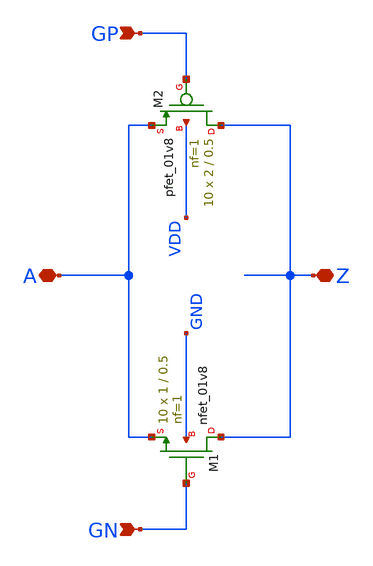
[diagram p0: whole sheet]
** sch_path: dacpassgate.sch
* Copyright 2021 Stefan Frederik Schippers
* Licensed under the Apache License, Version 2.0 (the "License");
* you may not use this file except in compliance with the License.
* You may obtain a copy of the License at
* https://www.apache.org/licenses/LICENSE-2.0
* Unless required by applicable law or agreed to in writing, software
* distributed under the License is distributed on an "AS IS" BASIS,
* WITHOUT WARRANTIES OR CONDITIONS OF ANY KIND, either express or implied.
* See the License for the specific language governing permissions and
* limitations under the License.
**.subckt dacpassgate A Z GP GN
*.iopin A
*.iopin Z
*.ipin GP
*.ipin GN
XM1 Z GN A GND sky130_fd_pr__nfet_01v8 L=0.5 W=1 nf=1 ad='int((nf+1)/2) * W/nf * 0.29' as='int((nf+2)/2) * W/nf * 0.29'
+ pd='2*int((nf+1)/2) * (W/nf + 0.29)' ps='2*int((nf+2)/2) * (W/nf + 0.29)' nrd='0.29 / W' nrs='0.29 / W'
+ sa=0 sb=0 sd=0 mult=10 m=10
XM2 Z GP A VDD sky130_fd_pr__pfet_01v8 L=0.5 W=2 nf=1 ad='int((nf+1)/2) * W/nf * 0.29' as='int((nf+2)/2) * W/nf * 0.29'
+ pd='2*int((nf+1)/2) * (W/nf + 0.29)' ps='2*int((nf+2)/2) * (W/nf + 0.29)' nrd='0.29 / W' nrs='0.29 / W'
+ sa=0 sb=0 sd=0 mult=10 m=10
**.ends
.end
